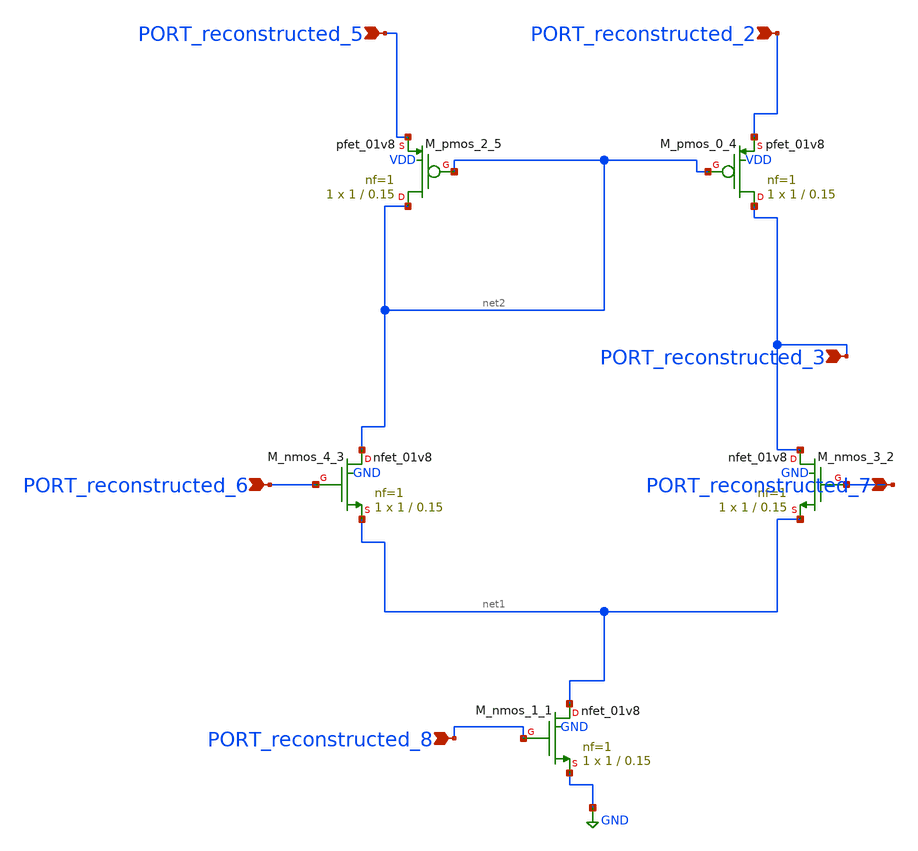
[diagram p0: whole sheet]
** sch_path: schematics/SchemGen/10_1109_ACCESS_2021_3072595_02_002.sch
**.subckt 10_1109_ACCESS_2021_3072595_02_002 PORT_reconstructed_3 PORT_reconstructed_2
*+ PORT_reconstructed_5 PORT_reconstructed_6 PORT_reconstructed_7 PORT_reconstructed_8
*.ipin PORT_reconstructed_3
*.ipin PORT_reconstructed_2
*.ipin PORT_reconstructed_5
*.ipin PORT_reconstructed_6
*.ipin PORT_reconstructed_7
*.ipin PORT_reconstructed_8
XM_nmos_1_1 net1 PORT_reconstructed_8 GND GND sky130_fd_pr__nfet_01v8 L=0.15 W=1 nf=1 ad='int((1 + 1)/2) * 1 / 1 * 0.29'
+ as='int((1 + 2)/2) * 1 / 1 * 0.29' pd='2*int((1 + 1)/2) * (1 / 1 + 0.29)' ps='2*int((1 + 2)/2) * (1 / 1 + 0.29)'
+ nrd='0.29 / 1 ' nrs='0.29 / 1 ' sa=0 sb=0 sd=0 mult=1 m=1
XM_nmos_3_2 PORT_reconstructed_3 PORT_reconstructed_7 net1 GND sky130_fd_pr__nfet_01v8 L=0.15 W=1 nf=1
+ ad='int((1 + 1)/2) * 1 / 1 * 0.29' as='int((1 + 2)/2) * 1 / 1 * 0.29' pd='2*int((1 + 1)/2) * (1 / 1 + 0.29)'
+ ps='2*int((1 + 2)/2) * (1 / 1 + 0.29)' nrd='0.29 / 1 ' nrs='0.29 / 1 ' sa=0 sb=0 sd=0 mult=1 m=1
XM_nmos_4_3 net2 PORT_reconstructed_6 net1 GND sky130_fd_pr__nfet_01v8 L=0.15 W=1 nf=1 ad='int((1 + 1)/2) * 1 / 1 * 0.29'
+ as='int((1 + 2)/2) * 1 / 1 * 0.29' pd='2*int((1 + 1)/2) * (1 / 1 + 0.29)' ps='2*int((1 + 2)/2) * (1 / 1 + 0.29)'
+ nrd='0.29 / 1 ' nrs='0.29 / 1 ' sa=0 sb=0 sd=0 mult=1 m=1
XM_pmos_0_4 PORT_reconstructed_3 net2 PORT_reconstructed_2 VDD sky130_fd_pr__pfet_01v8 L=0.15 W=1 nf=1
+ ad='int((1 + 1)/2) * 1 / 1 * 0.29' as='int((1 + 2)/2) * 1 / 1 * 0.29' pd='2*int((1 + 1)/2) * (1 / 1 + 0.29)'
+ ps='2*int((1 + 2)/2) * (1 / 1 + 0.29)' nrd='0.29 / 1 ' nrs='0.29 / 1 ' sa=0 sb=0 sd=0 mult=1 m=1
XM_pmos_2_5 net2 net2 PORT_reconstructed_5 VDD sky130_fd_pr__pfet_01v8 L=0.15 W=1 nf=1 ad='int((1 + 1)/2) * 1 / 1 * 0.29'
+ as='int((1 + 2)/2) * 1 / 1 * 0.29' pd='2*int((1 + 1)/2) * (1 / 1 + 0.29)' ps='2*int((1 + 2)/2) * (1 / 1 + 0.29)'
+ nrd='0.29 / 1 ' nrs='0.29 / 1 ' sa=0 sb=0 sd=0 mult=1 m=1
**.ends
.GLOBAL GND
.end
